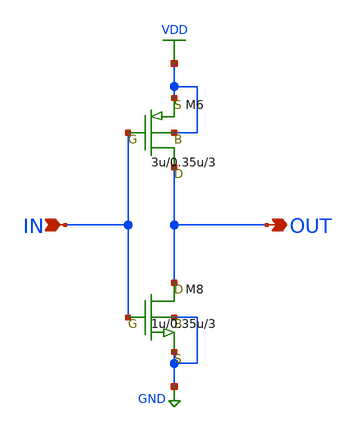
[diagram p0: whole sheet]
** sch_path: LR_hasegawa/LR_Work2/symbol/INVERTER3.sch
**.subckt INVERTER3 OUT IN
*.opin OUT
*.ipin IN
M6 OUT IN VDD VDD pch w=3u l=0.35u as=5.6p ps=9u ad=5.6p pd=9u m=3
M8 OUT IN GND GND nch w=1u l=0.35u as=2.8p ps=5.5u ad=2.8p pd=5.5u m=3
**.ends
.GLOBAL VDD
.GLOBAL GND
.end
